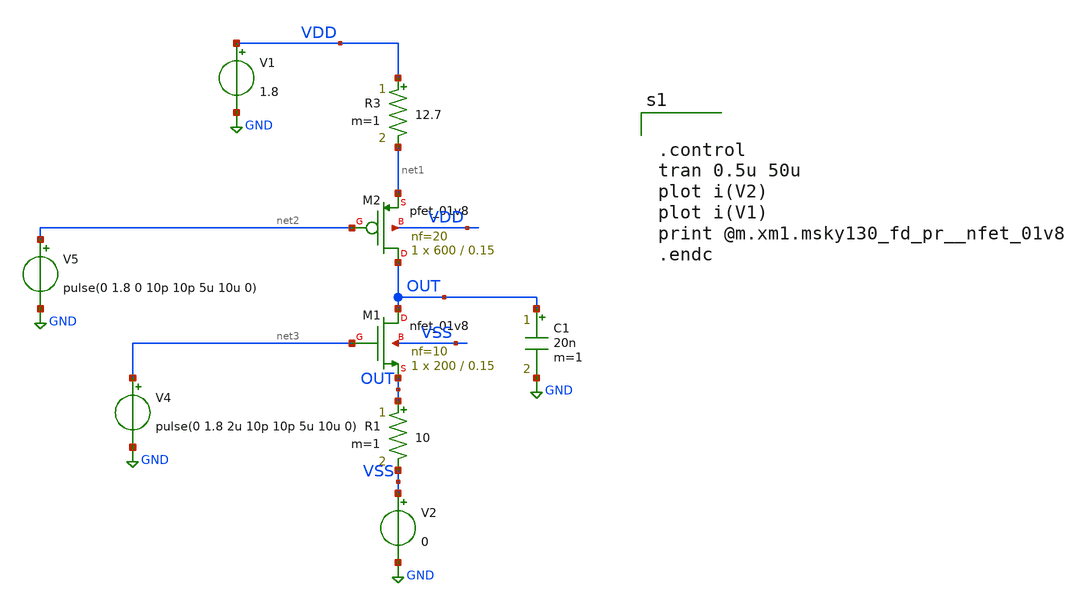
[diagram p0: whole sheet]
** sch_path: xschem/DC_DC_Converter_xschem/OTHERS/DC_DC_Converter1/current_pump/current_pump_tb1.sch
**.subckt current_pump_tb1
R3 VDD net1 12.7 m=1
R1 OUT VSS 10 m=1
XM1 OUT net3 OUT VSS sky130_fd_pr__nfet_01v8 L=0.15 W=200 nf=10 ad='int((nf+1)/2) * W/nf * 0.29' as='int((nf+2)/2) * W/nf * 0.29'
+ pd='2*int((nf+1)/2) * (W/nf + 0.29)' ps='2*int((nf+2)/2) * (W/nf + 0.29)' nrd='0.29 / W' nrs='0.29 / W'
+ sa=0 sb=0 sd=0 mult=1 m=1
XM2 OUT net2 net1 VDD sky130_fd_pr__pfet_01v8 L=0.15 W=600 nf=20 ad='int((nf+1)/2) * W/nf * 0.29' as='int((nf+2)/2) * W/nf * 0.29'
+ pd='2*int((nf+1)/2) * (W/nf + 0.29)' ps='2*int((nf+2)/2) * (W/nf + 0.29)' nrd='0.29 / W' nrs='0.29 / W'
+ sa=0 sb=0 sd=0 mult=1 m=1
C1 OUT GND 20n m=1
V5 net2 GND pulse(0 1.8 0 10p 10p 5u 10u 0)
V4 net3 GND pulse(0 1.8 2u 10p 10p 5u 10u 0)
V1 VDD GND 1.8
V2 VSS GND 0
**** begin user architecture code


.control
tran 0.5u 50u
plot i(V2)
plot i(V1)
print @m.xm1.msky130_fd_pr__nfet_01v8
.endc



** opencircuitdesign pdks install
.lib $::SKYWATER_MODELS/sky130.lib.spice tt


**** end user architecture code
**.ends
.GLOBAL GND
.end
